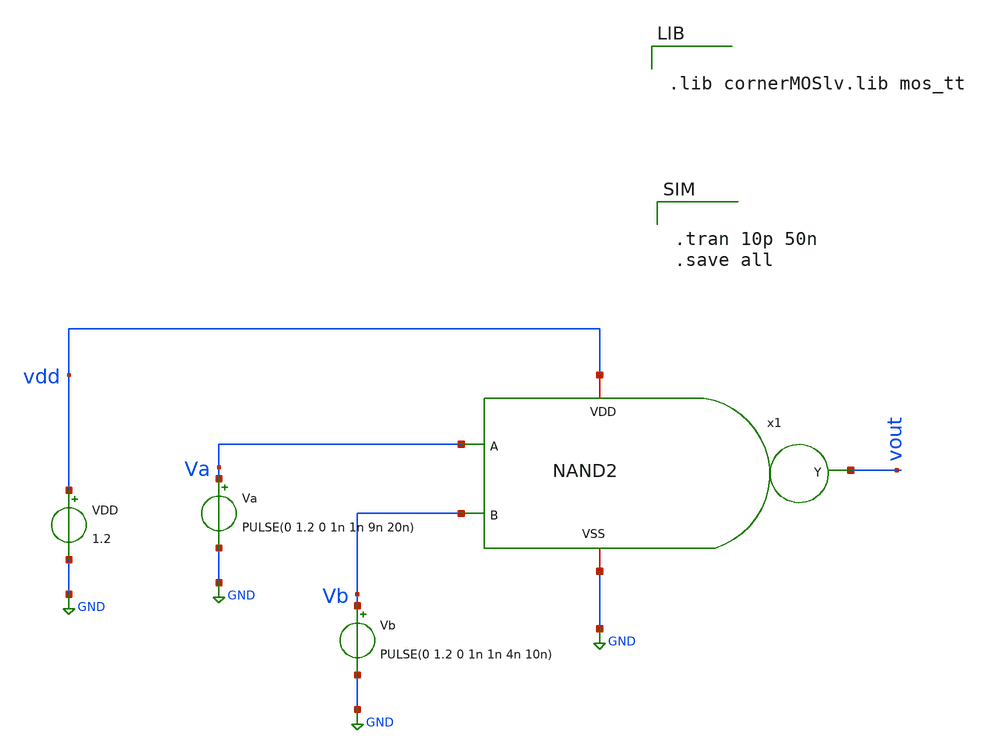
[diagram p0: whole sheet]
** sch_path: LogicGate/inverter_sym.sch
**.subckt inverter_sym
Va Va GND PULSE(0 1.2 0 1n 1n 9n 20n)
VDD vdd GND 1.2
x1 vdd Va vout Vb GND NAND2
Vb Vb GND PULSE(0 1.2 0 1n 1n 4n 10n)
**** begin user architecture code


.lib cornerMOSlv.lib mos_tt




.tran 10p 50n
.save all


**** end user architecture code
**.ends

* expanding   symbol:  /foss/designs/LogicGate/NAND2.sym # of pins=5
** sym_path: LogicGate/NAND2.sym
** sch_path: LogicGate/NAND2.sch
.subckt NAND2 VDD A Y B VSS
*.opin Y
*.iopin VDD
*.iopin VSS
*.ipin A
*.ipin B
XXM2 Y B VDD VDD sg13_lv_pmos w=0.15u l=0.13u ng=1 m=1 mm_ok=1
XXM1 Y A VDD VDD sg13_lv_pmos w=0.15u l=0.13u ng=1 m=1 mm_ok=1
XXM3 Y A net1 VSS sg13_lv_nmos w=0.15u l=0.13u ng=1 m=1 mm_ok=1
XXM4 net1 B VSS VSS sg13_lv_nmos w=0.15u l=0.13u ng=1 m=1 mm_ok=1
.ends

.GLOBAL GND
.end
